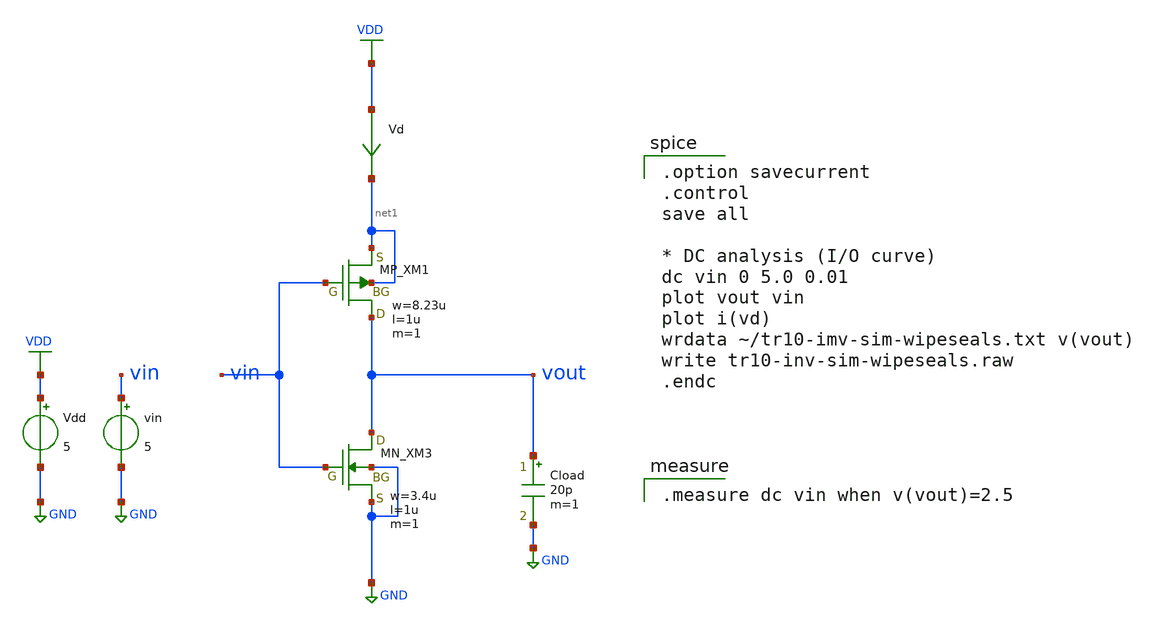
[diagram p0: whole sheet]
** sch_path: member_project/inverter/wipeseals/misc/tr10-inv-sim-trsize-wipeseals.sch
**.subckt tr10-inv-sim-trsize-wipeseals
Vdd VDD GND 5
vin vin GND 5
Vd VDD net1 0
.save i(vd)
Cload vout GND 20p m=1
XM1 vout vin net1 net1 PMOS w=8.23u l=1u as=0 ad=0 ps=0 pd=0 nrd=0 nrs=0 m=1
XM3 vout vin GND GND NMOS w=3.4u l=1u as=0 ad=0 ps=0 pd=0 nrd=0 nrs=0 m=1
**** begin user architecture code
 .include $::LIB/../ip62_models

.option savecurrent
.control
save all

* DC analysis (I/O curve)
dc vin 0 5.0 0.01
plot vout vin
plot i(vd)
wrdata ~/tr10-imv-sim-wipeseals.txt v(vout)
write tr10-inv-sim-wipeseals.raw
.endc



.measure dc vin when v(vout)=2.5

**** end user architecture code
**.ends
.GLOBAL VDD
.GLOBAL GND
.end
